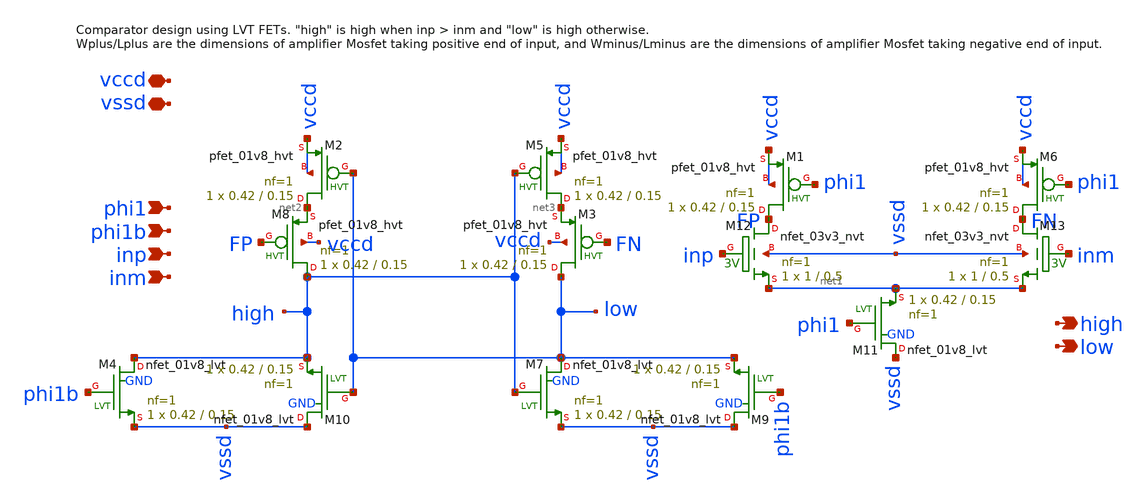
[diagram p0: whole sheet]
** sch_path: xschem/comparator_latest/comparator_single_tail.sch
**.subckt comparator_single_tail phi1 high phi1b inp inm low vccd vssd
*.ipin phi1
*.opin high
*.ipin phi1b
*.ipin inp
*.ipin inm
*.opin low
*.iopin vccd
*.iopin vssd
XM4 high phi1b vssd GND sky130_fd_pr__nfet_01v8_lvt L=0.15 W=0.42 nf=1 ad='int((nf+1)/2) * W/nf * 0.29'
+ as='int((nf+2)/2) * W/nf * 0.29' pd='2*int((nf+1)/2) * (W/nf + 0.29)' ps='2*int((nf+2)/2) * (W/nf + 0.29)'
+ nrd='0.29 / W' nrs='0.29 / W' sa=0 sb=0 sd=0 mult=1 m=1
XM7 low high vssd GND sky130_fd_pr__nfet_01v8_lvt L=0.15 W=0.42 nf=1 ad='int((nf+1)/2) * W/nf * 0.29'
+ as='int((nf+2)/2) * W/nf * 0.29' pd='2*int((nf+1)/2) * (W/nf + 0.29)' ps='2*int((nf+2)/2) * (W/nf + 0.29)'
+ nrd='0.29 / W' nrs='0.29 / W' sa=0 sb=0 sd=0 mult=1 m=1
XM9 vssd phi1b low GND sky130_fd_pr__nfet_01v8_lvt L=0.15 W=0.42 nf=1 ad='int((nf+1)/2) * W/nf * 0.29'
+ as='int((nf+2)/2) * W/nf * 0.29' pd='2*int((nf+1)/2) * (W/nf + 0.29)' ps='2*int((nf+2)/2) * (W/nf + 0.29)'
+ nrd='0.29 / W' nrs='0.29 / W' sa=0 sb=0 sd=0 mult=1 m=1
XM10 vssd low high GND sky130_fd_pr__nfet_01v8_lvt L=0.15 W=0.42 nf=1 ad='int((nf+1)/2) * W/nf * 0.29'
+ as='int((nf+2)/2) * W/nf * 0.29' pd='2*int((nf+1)/2) * (W/nf + 0.29)' ps='2*int((nf+2)/2) * (W/nf + 0.29)'
+ nrd='0.29 / W' nrs='0.29 / W' sa=0 sb=0 sd=0 mult=1 m=1
XM11 vssd phi1 net1 GND sky130_fd_pr__nfet_01v8_lvt L=0.15 W=0.42 nf=1 ad='int((nf+1)/2) * W/nf * 0.29'
+ as='int((nf+2)/2) * W/nf * 0.29' pd='2*int((nf+1)/2) * (W/nf + 0.29)' ps='2*int((nf+2)/2) * (W/nf + 0.29)'
+ nrd='0.29 / W' nrs='0.29 / W' sa=0 sb=0 sd=0 mult=1 m=1
XM12 FP inp net1 vssd sky130_fd_pr__nfet_03v3_nvt L=0.5 W=1 nf=1 ad='int((nf+1)/2) * W/nf * 0.29' as='int((nf+2)/2) * W/nf * 0.29'
+ pd='2*int((nf+1)/2) * (W/nf + 0.29)' ps='2*int((nf+2)/2) * (W/nf + 0.29)' nrd='0.29 / W' nrs='0.29 / W'
+ sa=0 sb=0 sd=0 mult=1 m=1
XM13 FN inm net1 vssd sky130_fd_pr__nfet_03v3_nvt L=0.5 W=1 nf=1 ad='int((nf+1)/2) * W/nf * 0.29' as='int((nf+2)/2) * W/nf * 0.29'
+ pd='2*int((nf+1)/2) * (W/nf + 0.29)' ps='2*int((nf+2)/2) * (W/nf + 0.29)' nrd='0.29 / W' nrs='0.29 / W'
+ sa=0 sb=0 sd=0 mult=1 m=1
XM6 FN phi1 vccd vccd sky130_fd_pr__pfet_01v8_hvt L=0.15 W=0.42 nf=1 ad='int((nf+1)/2) * W/nf * 0.29'
+ as='int((nf+2)/2) * W/nf * 0.29' pd='2*int((nf+1)/2) * (W/nf + 0.29)' ps='2*int((nf+2)/2) * (W/nf + 0.29)'
+ nrd='0.29 / W' nrs='0.29 / W' sa=0 sb=0 sd=0 mult=1 m=1
XM1 FP phi1 vccd vccd sky130_fd_pr__pfet_01v8_hvt L=0.15 W=0.42 nf=1 ad='int((nf+1)/2) * W/nf * 0.29'
+ as='int((nf+2)/2) * W/nf * 0.29' pd='2*int((nf+1)/2) * (W/nf + 0.29)' ps='2*int((nf+2)/2) * (W/nf + 0.29)'
+ nrd='0.29 / W' nrs='0.29 / W' sa=0 sb=0 sd=0 mult=1 m=1
XM2 net2 low vccd vccd sky130_fd_pr__pfet_01v8_hvt L=0.15 W=0.42 nf=1 ad='int((nf+1)/2) * W/nf * 0.29'
+ as='int((nf+2)/2) * W/nf * 0.29' pd='2*int((nf+1)/2) * (W/nf + 0.29)' ps='2*int((nf+2)/2) * (W/nf + 0.29)'
+ nrd='0.29 / W' nrs='0.29 / W' sa=0 sb=0 sd=0 mult=1 m=1
XM3 low FN net3 vccd sky130_fd_pr__pfet_01v8_hvt L=0.15 W=0.42 nf=1 ad='int((nf+1)/2) * W/nf * 0.29'
+ as='int((nf+2)/2) * W/nf * 0.29' pd='2*int((nf+1)/2) * (W/nf + 0.29)' ps='2*int((nf+2)/2) * (W/nf + 0.29)'
+ nrd='0.29 / W' nrs='0.29 / W' sa=0 sb=0 sd=0 mult=1 m=1
XM5 net3 high vccd vccd sky130_fd_pr__pfet_01v8_hvt L=0.15 W=0.42 nf=1 ad='int((nf+1)/2) * W/nf * 0.29'
+ as='int((nf+2)/2) * W/nf * 0.29' pd='2*int((nf+1)/2) * (W/nf + 0.29)' ps='2*int((nf+2)/2) * (W/nf + 0.29)'
+ nrd='0.29 / W' nrs='0.29 / W' sa=0 sb=0 sd=0 mult=1 m=1
XM8 high FP net2 vccd sky130_fd_pr__pfet_01v8_hvt L=0.15 W=0.42 nf=1 ad='int((nf+1)/2) * W/nf * 0.29'
+ as='int((nf+2)/2) * W/nf * 0.29' pd='2*int((nf+1)/2) * (W/nf + 0.29)' ps='2*int((nf+2)/2) * (W/nf + 0.29)'
+ nrd='0.29 / W' nrs='0.29 / W' sa=0 sb=0 sd=0 mult=1 m=1
**.ends
.end
